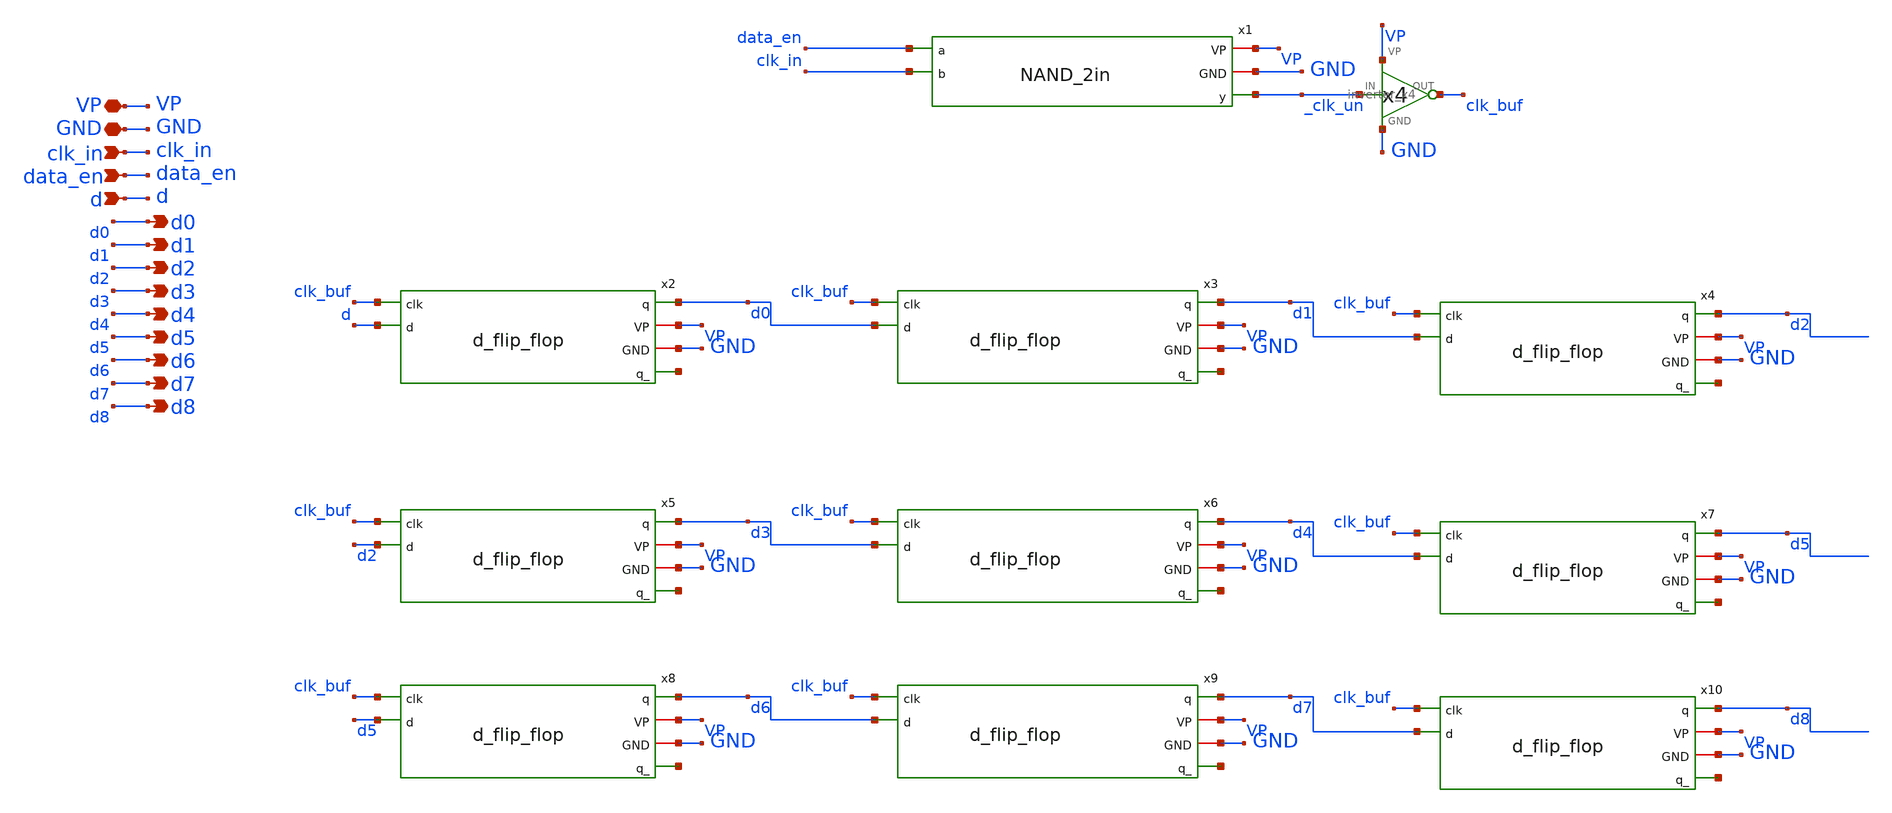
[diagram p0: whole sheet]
** sch_path: schematics/divider/schematics/input_register.sch
**.subckt input_register VP clk_in GND data_en d d0 d2 d3 d4 d5 d6 d7 d1 d8
*.iopin VP
*.ipin clk_in
*.iopin GND
*.ipin data_en
*.ipin d
*.opin d0
*.opin d2
*.opin d3
*.opin d4
*.opin d5
*.opin d6
*.opin d7
*.opin d1
*.opin d8
x2 d0 VP GND net1 clk_buf d d_flip_flop
x3 d1 VP GND net2 clk_buf d0 d_flip_flop
x4 d2 VP GND net3 clk_buf d1 d_flip_flop
x5 d3 VP GND net4 clk_buf d2 d_flip_flop
x6 d4 VP GND net5 clk_buf d3 d_flip_flop
x7 d5 VP GND net6 clk_buf d4 d_flip_flop
x8 d6 VP GND net7 clk_buf d5 d_flip_flop
x9 d7 VP GND net8 clk_buf d6 d_flip_flop
x10 d8 VP GND net9 clk_buf d7 d_flip_flop
x1 VP GND data_en _clk_un clk_in NAND_2in
x11 _clk_un clk_buf VP GND inverter_x4
**.ends
.end
